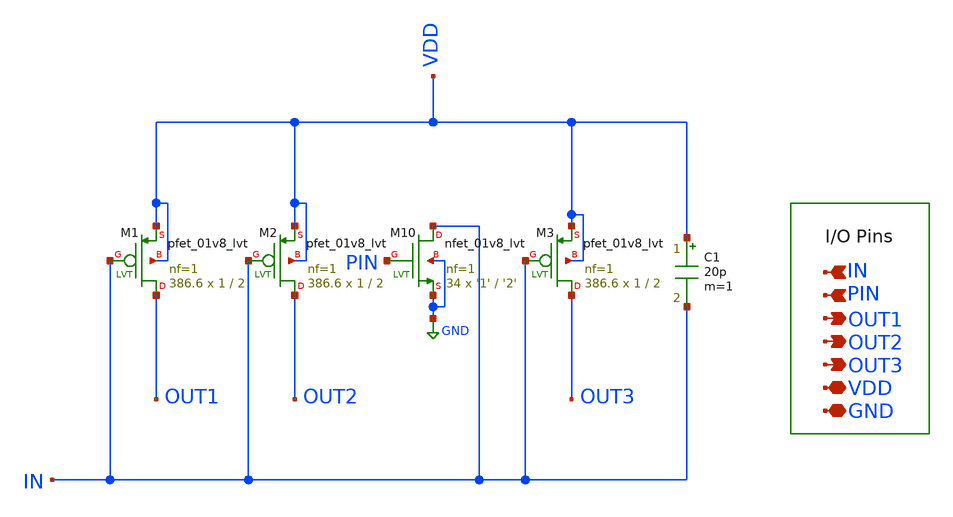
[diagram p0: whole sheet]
** sch_path: bandgap_sky130_v1/current_3_mirror-ckt.sch
**.subckt current_3_mirror-ckt IN OUT2 VDD GND OUT3 OUT1 PIN
*.ipin IN
*.opin OUT2
*.iopin VDD
*.iopin GND
*.opin OUT3
*.opin OUT1
*.ipin PIN
C1 VDD IN 20p m=1
XM1 OUT1 IN VDD VDD sky130_fd_pr__pfet_01v8_lvt L=2 W=1 nf=1 ad='int((nf+1)/2) * W/nf * 0.29' as='int((nf+2)/2) * W/nf * 0.29'
+ pd='2*int((nf+1)/2) * (W/nf + 0.29)' ps='2*int((nf+2)/2) * (W/nf + 0.29)' nrd='0.29 / W' nrs='0.29 / W'
+ sa=0 sb=0 sd=0 mult=386.6 m=386.6
XM2 OUT2 IN VDD VDD sky130_fd_pr__pfet_01v8_lvt L=2 W=1 nf=1 ad='int((nf+1)/2) * W/nf * 0.29' as='int((nf+2)/2) * W/nf * 0.29'
+ pd='2*int((nf+1)/2) * (W/nf + 0.29)' ps='2*int((nf+2)/2) * (W/nf + 0.29)' nrd='0.29 / W' nrs='0.29 / W'
+ sa=0 sb=0 sd=0 mult=386.6 m=386.6
XM3 OUT3 IN VDD VDD sky130_fd_pr__pfet_01v8_lvt L=2 W=1 nf=1 ad='int((nf+1)/2) * W/nf * 0.29' as='int((nf+2)/2) * W/nf * 0.29'
+ pd='2*int((nf+1)/2) * (W/nf + 0.29)' ps='2*int((nf+2)/2) * (W/nf + 0.29)' nrd='0.29 / W' nrs='0.29 / W'
+ sa=0 sb=0 sd=0 mult=386.6 m=386.6
XM10 IN PIN GND GND sky130_fd_pr__nfet_01v8_lvt L='2' W='1' nf=1 ad='int((nf+1)/2) * W/nf * 0.29' as='int((nf+2)/2) * W/nf * 0.29'
+ pd='2*int((nf+1)/2) * (W/nf + 0.29)' ps='2*int((nf+2)/2) * (W/nf + 0.29)' nrd='0.29 / W' nrs='0.29 / W'
+ sa=0 sb=0 sd=0 mult=34 m=34
**.ends
.GLOBAL GND
.end
